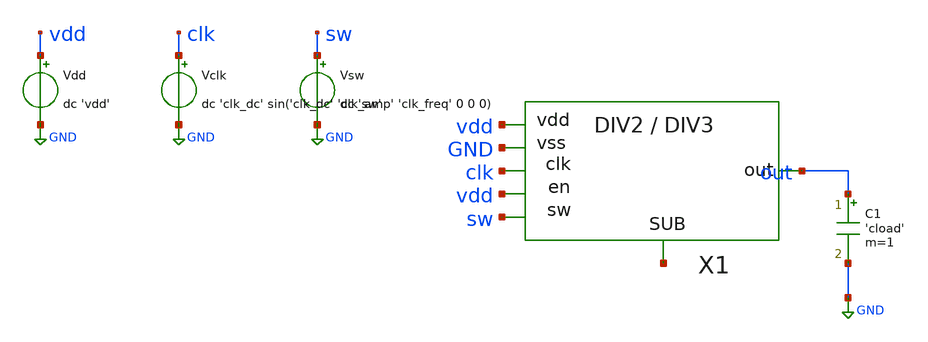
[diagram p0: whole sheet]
** sch_path: tb/divider/tb_divider_funct.sch
**.subckt tb_divider_funct
Vdd vdd GND dc 'vdd'
Vclk clk GND dc 'clk_dc' sin('clk_dc' 'clk_amp' 'clk_freq' 0 0 0)
Vsw sw GND dc 'sw'
X1 vdd GND sw out net1 vdd clk divider
C1 out GND 'cload' m=1
**** begin user architecture code


.include 'models_dir'/design.spice
.lib 'models_dir'/sm141064.spice 'mos_corner'
.lib 'models_dir'/sm141064.spice moscap_'mos_corner'
.option TEMP='temperature'
.option warn=1
.option rshunt=1e12
.control
save all
tran 5p 200n
set wr_singlescale
wrdata 'simpath'/'filename'_'N'.data v(clk) v(out) v(vdd) vdd#branch
quit
.endc


**** end user architecture code
**.ends
.GLOBAL GND
.end
